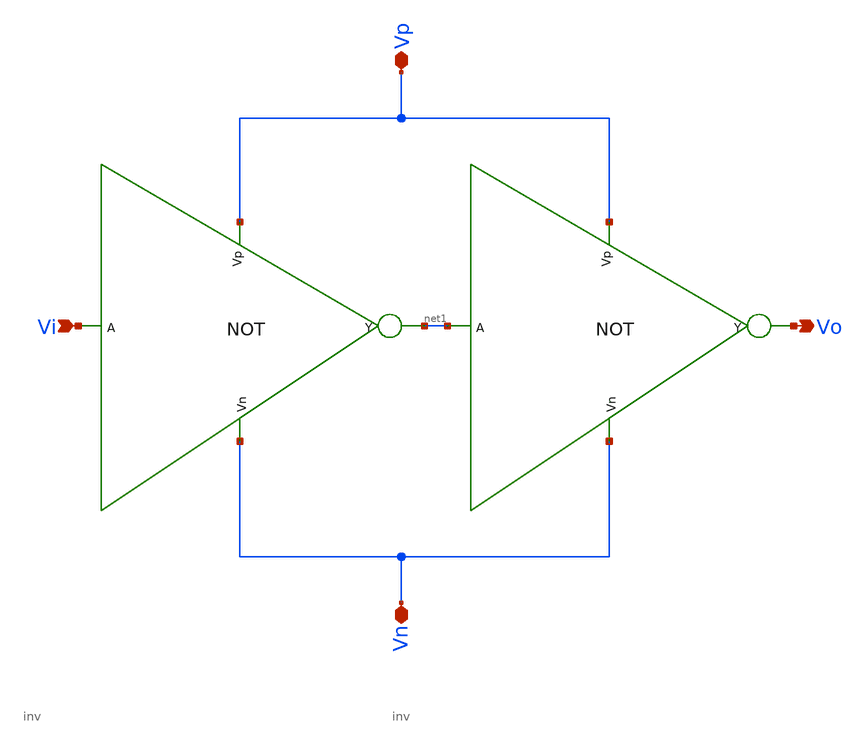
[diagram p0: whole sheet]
** sch_path: Buffer/Schematic/buffer.sch
**.subckt buffer Vi Vo Vp Vn
*.ipin Vi
*.opin Vo
*.iopin Vp
*.iopin Vn
x1 Vp Vi net1 Vn inv
x2 Vp net1 Vo Vn inv
**.ends

* expanding   symbol:  /home/chinmay/Desktop/Analog Design/CMOS/Inverter/Inverter Schema/inv.sym #
*+ of pins=4
** sym_path: Inverter/Schematic/inv.sym
** sch_path: Inverter/Schematic/inv.sch
.subckt inv Vp A Y Vn
*.ipin A
*.opin Y
*.ipin Vp
*.ipin Vn
XM1 Y A Vp Vp sky130_fd_pr__pfet_01v8 L=0.15 W=2 nf=1 ad='int((nf+1)/2) * W/nf * 0.29' as='int((nf+2)/2) * W/nf * 0.29'
+ pd='2*int((nf+1)/2) * (W/nf + 0.29)' ps='2*int((nf+2)/2) * (W/nf + 0.29)' nrd='0.29 / W' nrs='0.29 / W'
+ sa=0 sb=0 sd=0 mult=1 m=1
XM2 Y A Vn Vn sky130_fd_pr__nfet_01v8 L=0.15 W=1 nf=1 ad='int((nf+1)/2) * W/nf * 0.29' as='int((nf+2)/2) * W/nf * 0.29'
+ pd='2*int((nf+1)/2) * (W/nf + 0.29)' ps='2*int((nf+2)/2) * (W/nf + 0.29)' nrd='0.29 / W' nrs='0.29 / W'
+ sa=0 sb=0 sd=0 mult=1 m=1
.ends

.end
